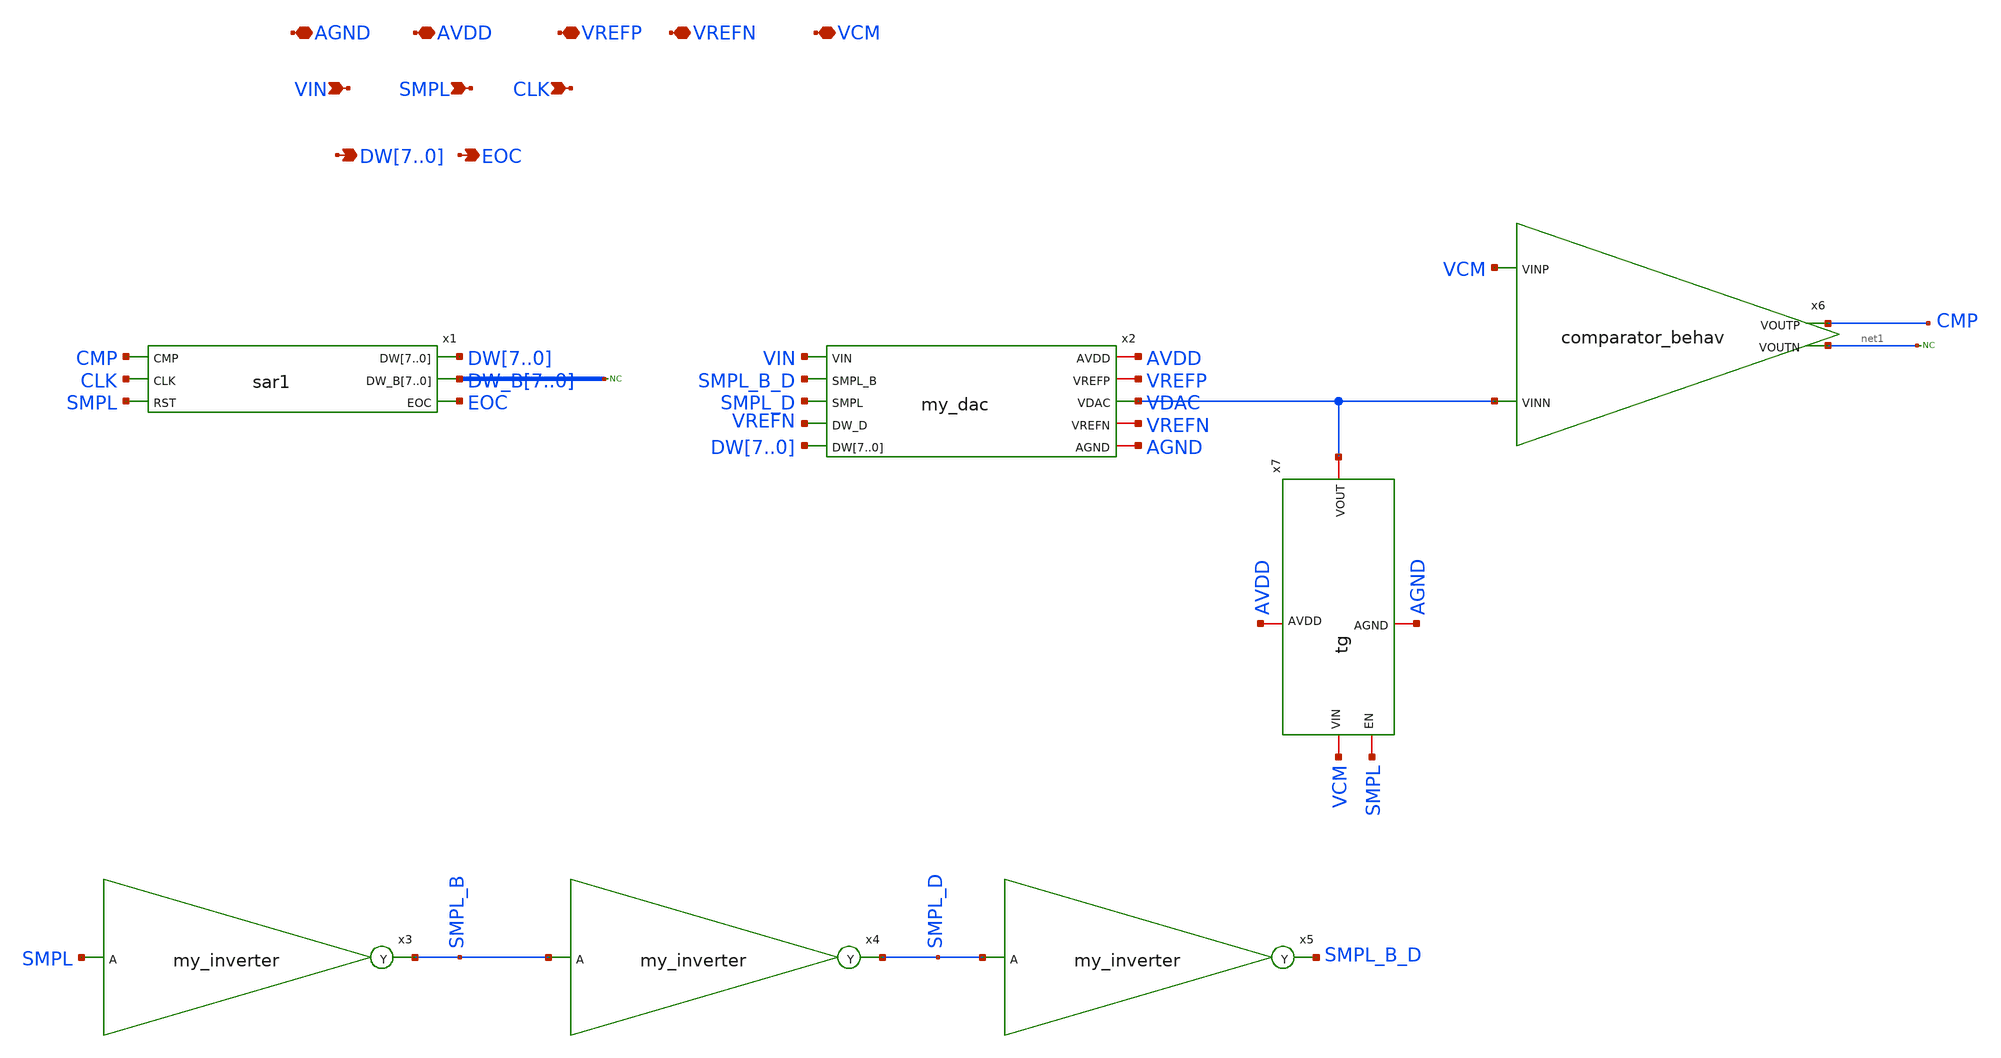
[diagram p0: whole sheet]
** sch_path: my_sar_adc.sch
**.subckt my_sar_adc AGND AVDD VREFP VREFN VCM VIN SMPL CLK DW7,DW6,DW5,DW4,DW3,DW2,DW1,DW0 EOC
*.iopin AGND
*.iopin AVDD
*.iopin VREFP
*.iopin VREFN
*.iopin VCM
*.ipin VIN
*.ipin SMPL
*.ipin CLK
*.opin DW7,DW6,DW5,DW4,DW3,DW2,DW1,DW0
*.opin EOC
x1 CMP CLK SMPL DW7 DW6 DW5 DW4 DW3 DW2 DW1 DW0 DW_B7 DW_B6 DW_B5 DW_B4 DW_B3 DW_B2 DW_B1 DW_B0 EOC
+ sar1
x2 AVDD AGND VREFN VREFP VDAC VIN SMPL_B_D SMPL_D VREFN DW7 DW6 DW5 DW4 DW3 DW2 DW1 DW0 my_dac
x3 SMPL_B SMPL my_inverter
x4 SMPL_D SMPL_B my_inverter
x5 SMPL_B_D SMPL_D my_inverter
x6 CMP VCM VDAC net1 comparator_behav
x7 SMPL AGND VDAC VCM AVDD tg
* noconn #net1
* noconn DW_B[7..0]
**.ends
.end
